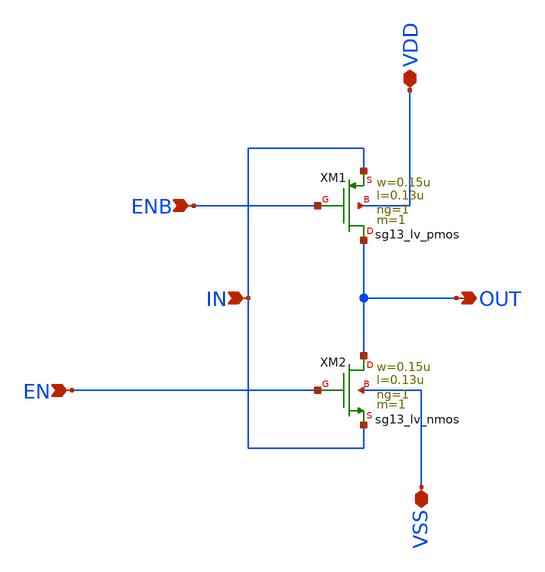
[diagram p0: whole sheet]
** sch_path: LogicGate/Tranmission.sch
**.subckt Tranmission IN OUT VDD VSS EN ENB
*.ipin IN
*.opin OUT
*.iopin VDD
*.iopin VSS
*.ipin EN
*.ipin ENB
XXM1 OUT ENB IN VDD sg13_lv_pmos w=0.15u l=0.13u ng=1 m=1 mm_ok=1
XXM2 OUT EN IN VSS sg13_lv_nmos w=0.15u l=0.13u ng=1 m=1 mm_ok=1
**.ends
.end
